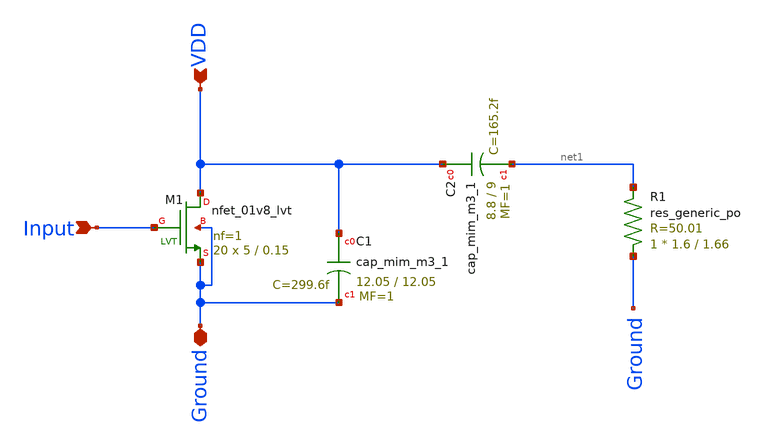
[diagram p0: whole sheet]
** sch_path: skywater_stuff/ECE631_RF_CMOS/Power_Amp_LVS_1.sch
**.subckt Power_Amp_LVS_1 Input VDD Ground
*.ipin Input
*.ipin VDD
*.iopin Ground
XM1 VDD Input Ground Ground sky130_fd_pr__nfet_01v8_lvt L=0.15 W=5 nf=1 ad='int((nf+1)/2) * W/nf * 0.29'
+ as='int((nf+2)/2) * W/nf * 0.29' pd='2*int((nf+1)/2) * (W/nf + 0.29)' ps='2*int((nf+2)/2) * (W/nf + 0.29)'
+ nrd='0.29 / W' nrs='0.29 / W' sa=0 sb=0 sd=0 mult=20 m=20
XC1 VDD Ground sky130_fd_pr__cap_mim_m3_1 W=12.05 L=12.05 MF=1 m=1
XR1 Ground net1 sky130_fd_pr__res_generic_po W=1.6 L=1.66 m=1
XC2 VDD net1 sky130_fd_pr__cap_mim_m3_1 W=8.8 L=9 MF=1 m=1
**.ends
.end
